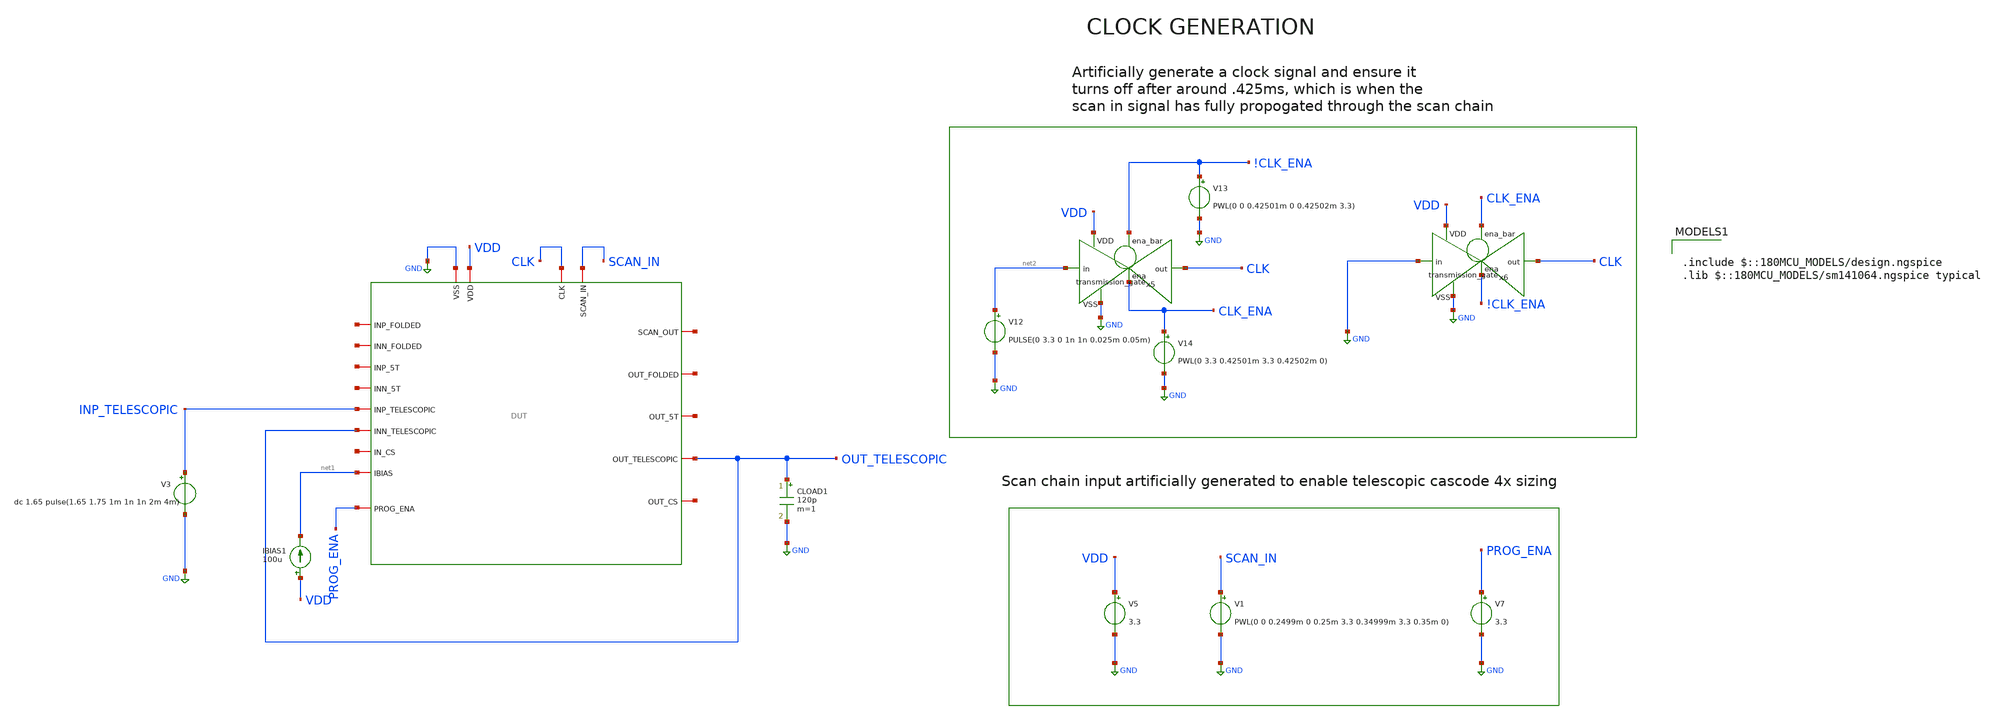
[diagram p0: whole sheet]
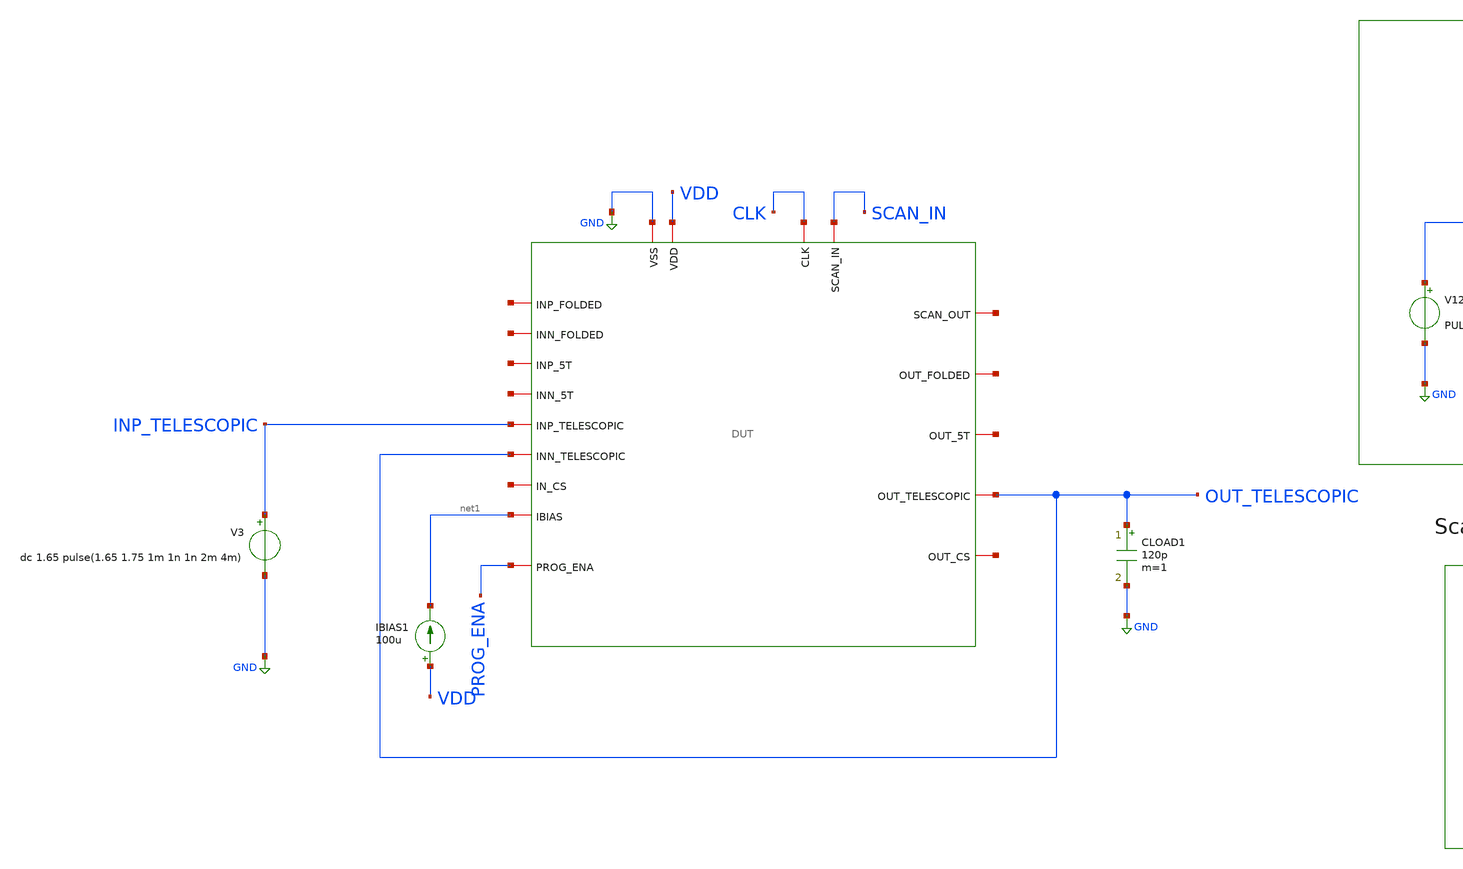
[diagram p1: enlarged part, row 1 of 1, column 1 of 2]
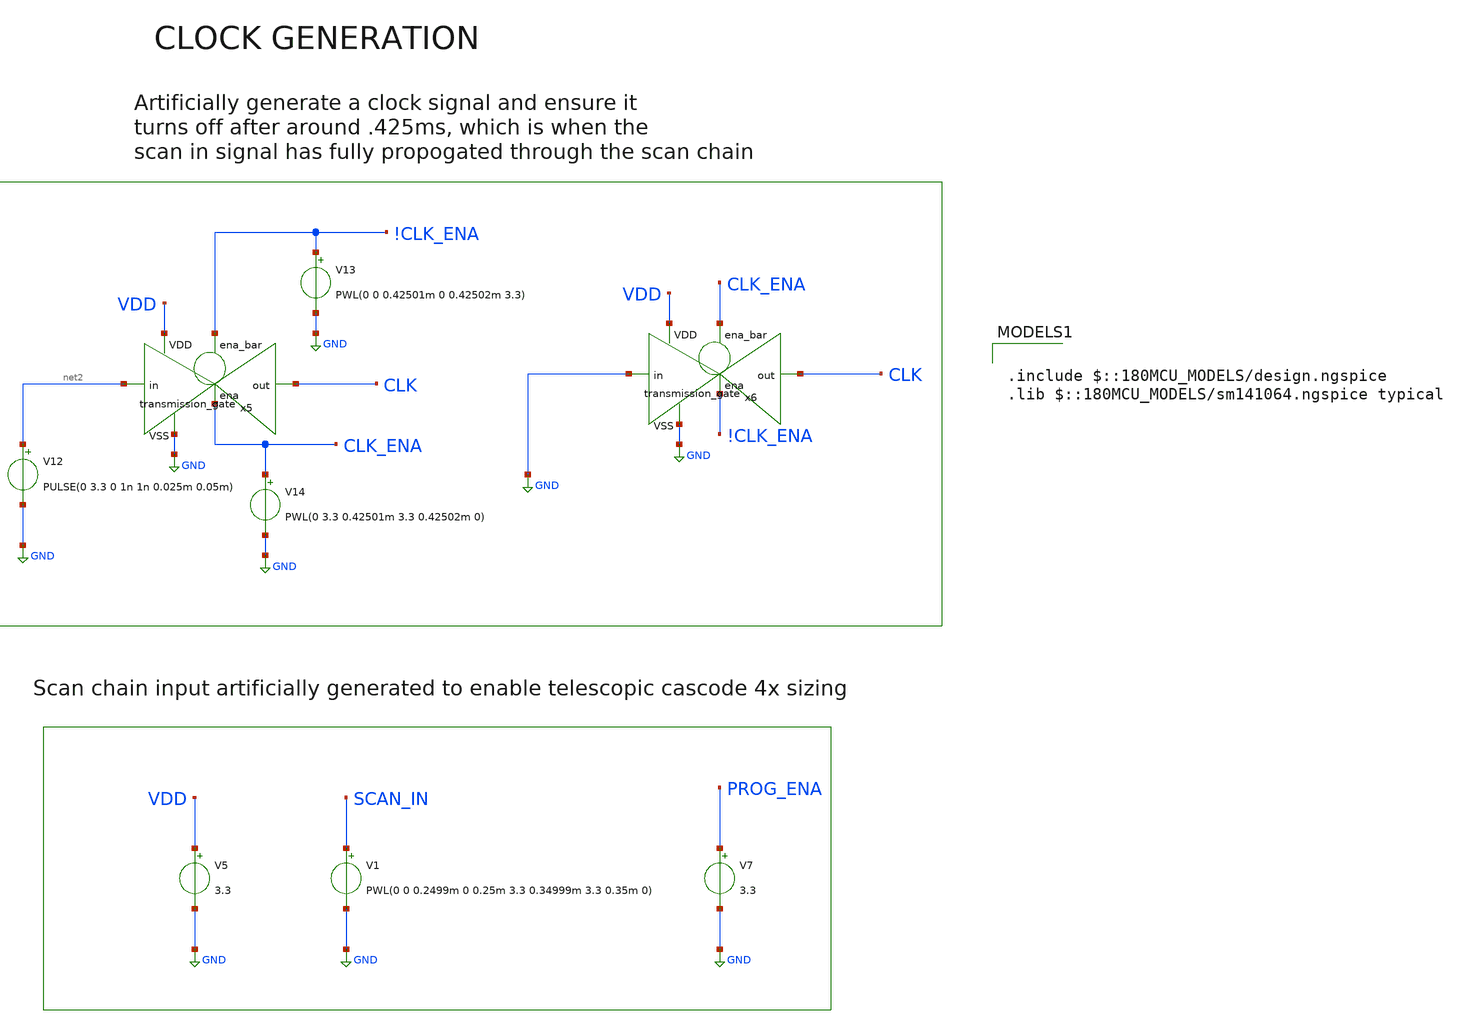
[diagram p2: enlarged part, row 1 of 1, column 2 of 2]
** sch_path: designs/libs/pex/tele/step_response/4x.sch
**.subckt 4x
CLOAD1 OUT_TELESCOPIC GND 120p m=1
V3 INP_TELESCOPIC GND dc 1.65 pulse(1.65 1.75 1m 1n 1n 2m 4m)
IBIAS1 VDD net1 100u
V5 VDD GND 3.3
V7 PROG_ENA GND 3.3
V12 net2 GND PULSE(0 3.3 0 1n 1n 0.025m 0.05m)
x5 !CLK_ENA VDD CLK net2 GND CLK_ENA transmission_gate
V13 !CLK_ENA GND PWL(0 0 0.42501m 0 0.42502m 3.3)
V14 CLK_ENA GND PWL(0 3.3 0.42501m 3.3 0.42502m 0)
x6 CLK_ENA VDD CLK GND GND !CLK_ENA transmission_gate
V1 SCAN_IN GND PWL(0 0 0.2499m 0 0.25m 3.3 0.34999m 3.3 0.35m 0)
x1 CLK net3 SCAN_IN GND VDD net4 net5 net6 net1 net7 net8 net9 INP_TELESCOPIC OUT_TELESCOPIC net10
+ net11 OUT_TELESCOPIC PROG_ENA DUT
**** begin user architecture code

.include $::180MCU_MODELS/design.ngspice
.lib $::180MCU_MODELS/sm141064.ngspice typical



.include /foss/designs/libs/pex/DUT.spice
.control
tran 1u 5m

plot v(out_telescopic) v(inp_telescopic)

meas tran v_before find v(out_telescopic) at=0.99m
meas tran v_after find v(out_telescopic) at=2.5m
print t_20
print t_80
let delta = v_after - v_before
let t20_val = v_before + 0.2 * delta
let t80_val = v_before + 0.8 * delta

meas tran t_20 when v(out_telescopic) = t20_val rise = 1 td=.99m
meas tran t_80 when v(out_telescopic) = t80_val rise = 1 td=.99m
let sr_rise = delta / (t_80 - t_20)
print sr_rise

meas tran t_20f when v(out_telescopic) = t80_val fall = 1 td=.99m
meas tran t_80f when v(out_telescopic) = t20_val fall = 1 td=.99m
let sr_fall = delta / (t_80f - t_20f)
print sr_fall

meas tran vpeak max v(out_telescopic) from=1m to=3m
let overshoot = (vpeak - v_after) / delta * 100
print overshoot

meas tran t_settle when v(out_telescopic) = v_after td = 1m rise = 1
let settling = t_settle - 1m
print settling

print v_before v_after delta
.endc


**** end user architecture code
**.ends

* expanding   symbol:  libs/core_digital/schem/transmission_gate.sym # of pins=6
** sym_path: designs/libs/core_digital/schem/transmission_gate.sym
** sch_path: designs/libs/core_digital/schem/transmission_gate.sch
.subckt transmission_gate ena_bar VDD out in VSS ena
*.ipin in
*.ipin ena_bar
*.ipin ena
*.ipin VSS
*.ipin VDD
*.opin out
XM1 in ena_bar out VDD pfet_03v3 L=0.28u W=0.22u nf=1 ad='int((nf+1)/2) * W/nf * 0.18u' as='int((nf+2)/2) * W/nf * 0.18u'
+ pd='2*int((nf+1)/2) * (W/nf + 0.18u)' ps='2*int((nf+2)/2) * (W/nf + 0.18u)' nrd='0.18u / W' nrs='0.18u / W'
+ sa=0 sb=0 sd=0 m=1
XM2 in ena out VSS nfet_03v3 L=0.28u W=0.22u nf=1 ad='int((nf+1)/2) * W/nf * 0.18u' as='int((nf+2)/2) * W/nf * 0.18u'
+ pd='2*int((nf+1)/2) * (W/nf + 0.18u)' ps='2*int((nf+2)/2) * (W/nf + 0.18u)' nrd='0.18u / W' nrs='0.18u / W'
+ sa=0 sb=0 sd=0 m=1
.ends

.GLOBAL GND
.end
